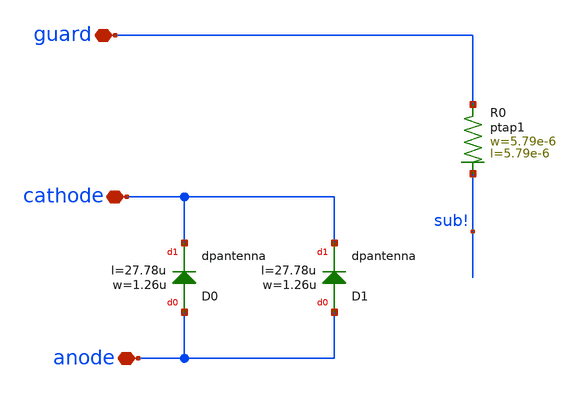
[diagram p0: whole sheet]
** sch_path: ihp-sg13g2/libs.ref/sg13g2_io/sch/xschem/sg13g2_DCPDiode.sch
**.subckt sg13g2_DCPDiode cathode anode guard
*.iopin cathode
*.iopin anode
*.iopin guard
XD0 anode cathode dpantenna l=27.78u w=1.26u
XD1 anode cathode dpantenna l=27.78u w=1.26u
XR0 guard sub! ptap1 R=17.29 w=5.79e-6 l=5.79e-6
**.ends
.end
